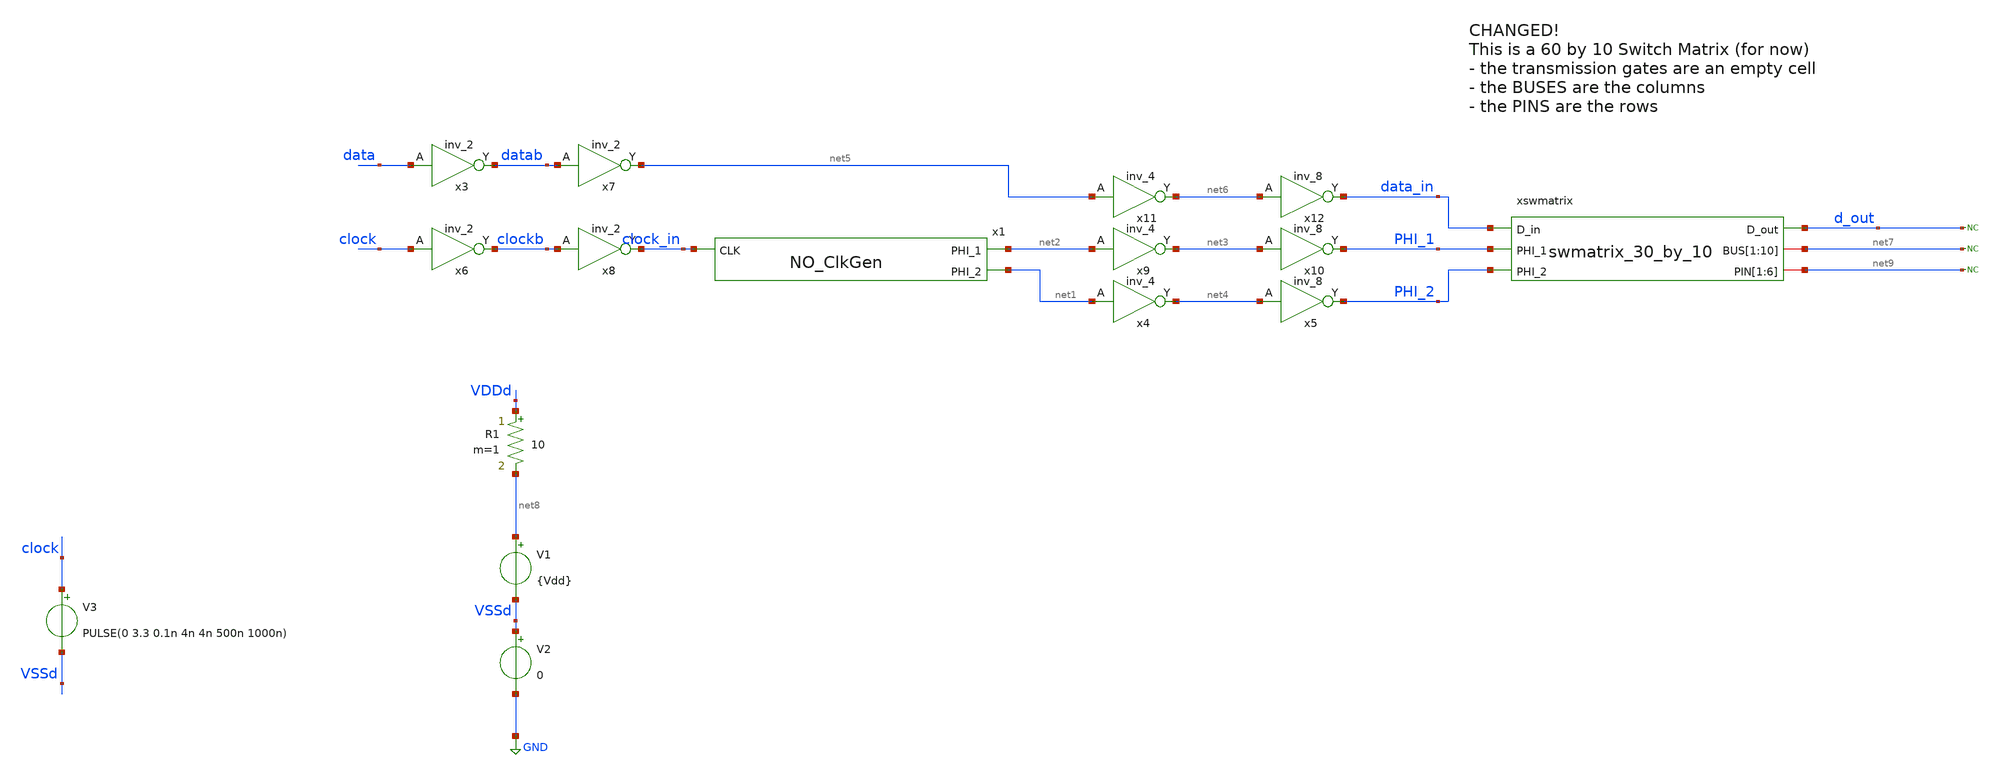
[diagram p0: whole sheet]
** sch_path: designs/Swmatrix.sch
**.subckt Swmatrix
x1 net1 clock_in net2 NO_ClkGen
xswmatrix data_in d_out PHI_1 PHI_2 net7 net7 net7 net7 net7 net7 net7 net7 net7 net7 net9 net9 net9
+ net9 net9 net9 swmatrix_30_by_10
V1 net8 VSSd {Vdd}
V2 VSSd GND 0
x3 data VSSd VDDd VSSd VDDd datab gf180mcu_fd_sc_mcu9t5v0__inv_2
x4 net1 VSSd VDDd VSSd VDDd net4 gf180mcu_fd_sc_mcu9t5v0__inv_4
x5 net4 VSSd VDDd VSSd VDDd PHI_2 gf180mcu_fd_sc_mcu9t5v0__inv_8
x6 clock VSSd VDDd VSSd VDDd clockb gf180mcu_fd_sc_mcu9t5v0__inv_2
x7 datab VSSd VDDd VSSd VDDd net5 gf180mcu_fd_sc_mcu9t5v0__inv_2
x8 clockb VSSd VDDd VSSd VDDd clock_in gf180mcu_fd_sc_mcu9t5v0__inv_2
x9 net2 VSSd VDDd VSSd VDDd net3 gf180mcu_fd_sc_mcu9t5v0__inv_4
x10 net3 VSSd VDDd VSSd VDDd PHI_1 gf180mcu_fd_sc_mcu9t5v0__inv_8
x11 net5 VSSd VDDd VSSd VDDd net6 gf180mcu_fd_sc_mcu9t5v0__inv_4
x12 net6 VSSd VDDd VSSd VDDd data_in gf180mcu_fd_sc_mcu9t5v0__inv_8
* noconn d_out
* noconn #net7
R1 VDDd net8 10 m=1
* noconn #net9
V3 clock VSSd PULSE(0 3.3 0.1n 4n 4n 500n 1000n)
**** begin user architecture code

.include /foss/pdks/gf180mcuD/libs.ref/gf180mcu_fd_sc_mcu9t5v0/spice/gf180mcu_fd_sc_mcu9t5v0.spice
.include $::180MCU_MODELS/design.ngspice
.lib $::180MCU_MODELS/sm141064.ngspice typical



.control

    save all
    TRAN 2n 61000n
    write Swmatrix.raw

.endc




.param VDD = 3.3

.global VDDd VSSd

* data
aclock [ clock_node ] clock_vector
.model clock_vector d_source(input_file="/foss/designs/libs/data_source/data_swmatrix5_10.txt")
* convert digital signals to analog
aconvert [ clock_node ] [  data ] dac_in
.model dac_in dac_bridge (out_low=0V out_high=3.3V t_rise=4ns t_fall=4ns)


**** end user architecture code
**.ends
.GLOBAL GND
.end
